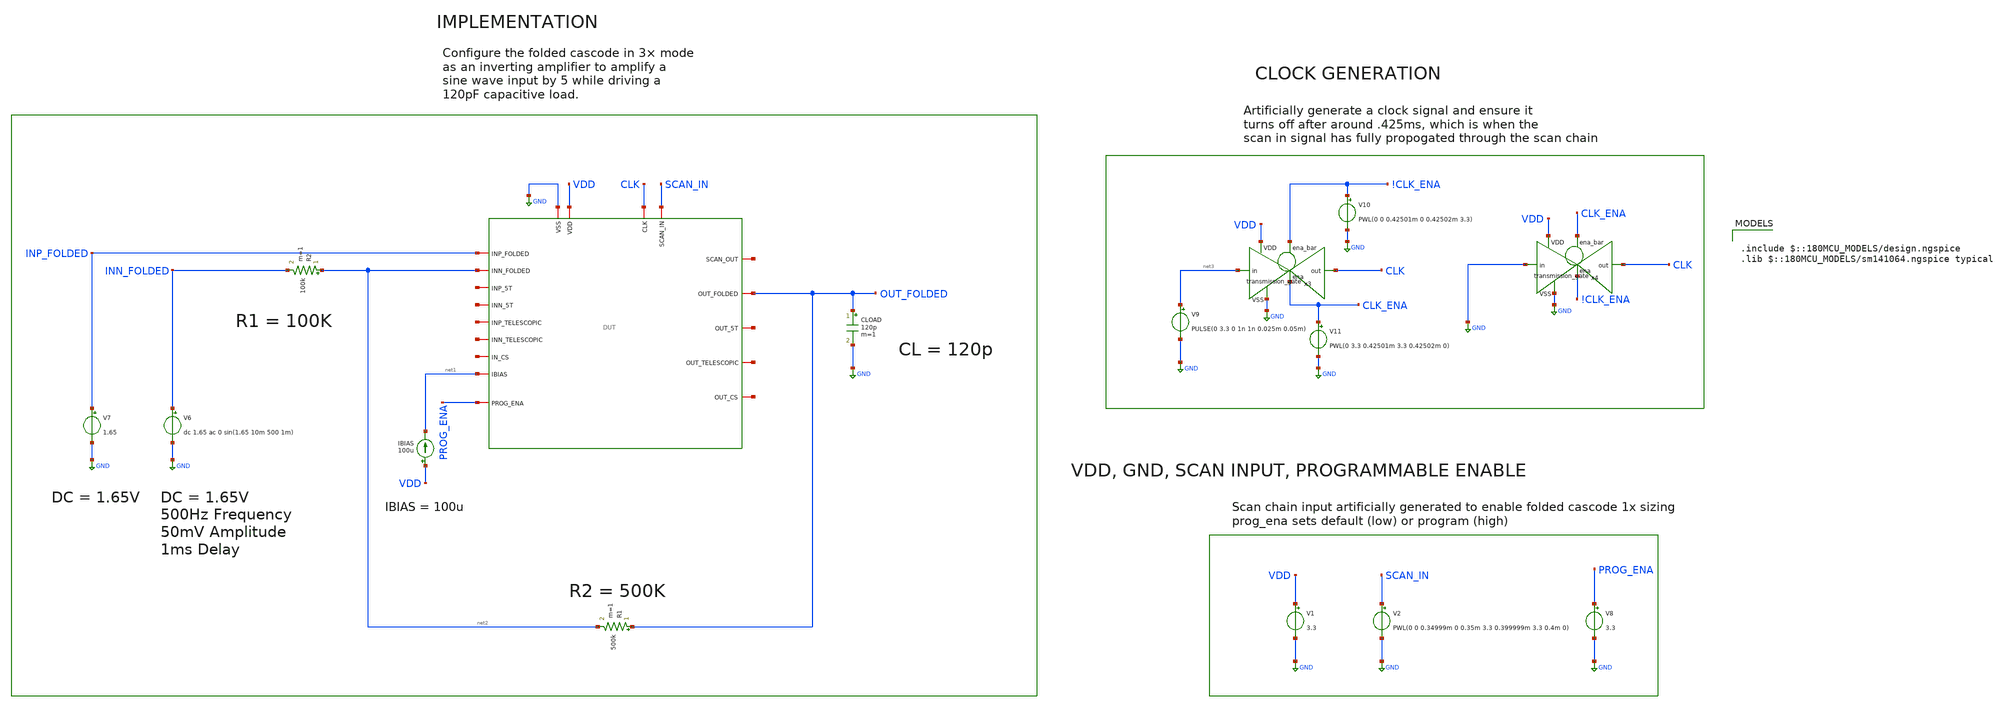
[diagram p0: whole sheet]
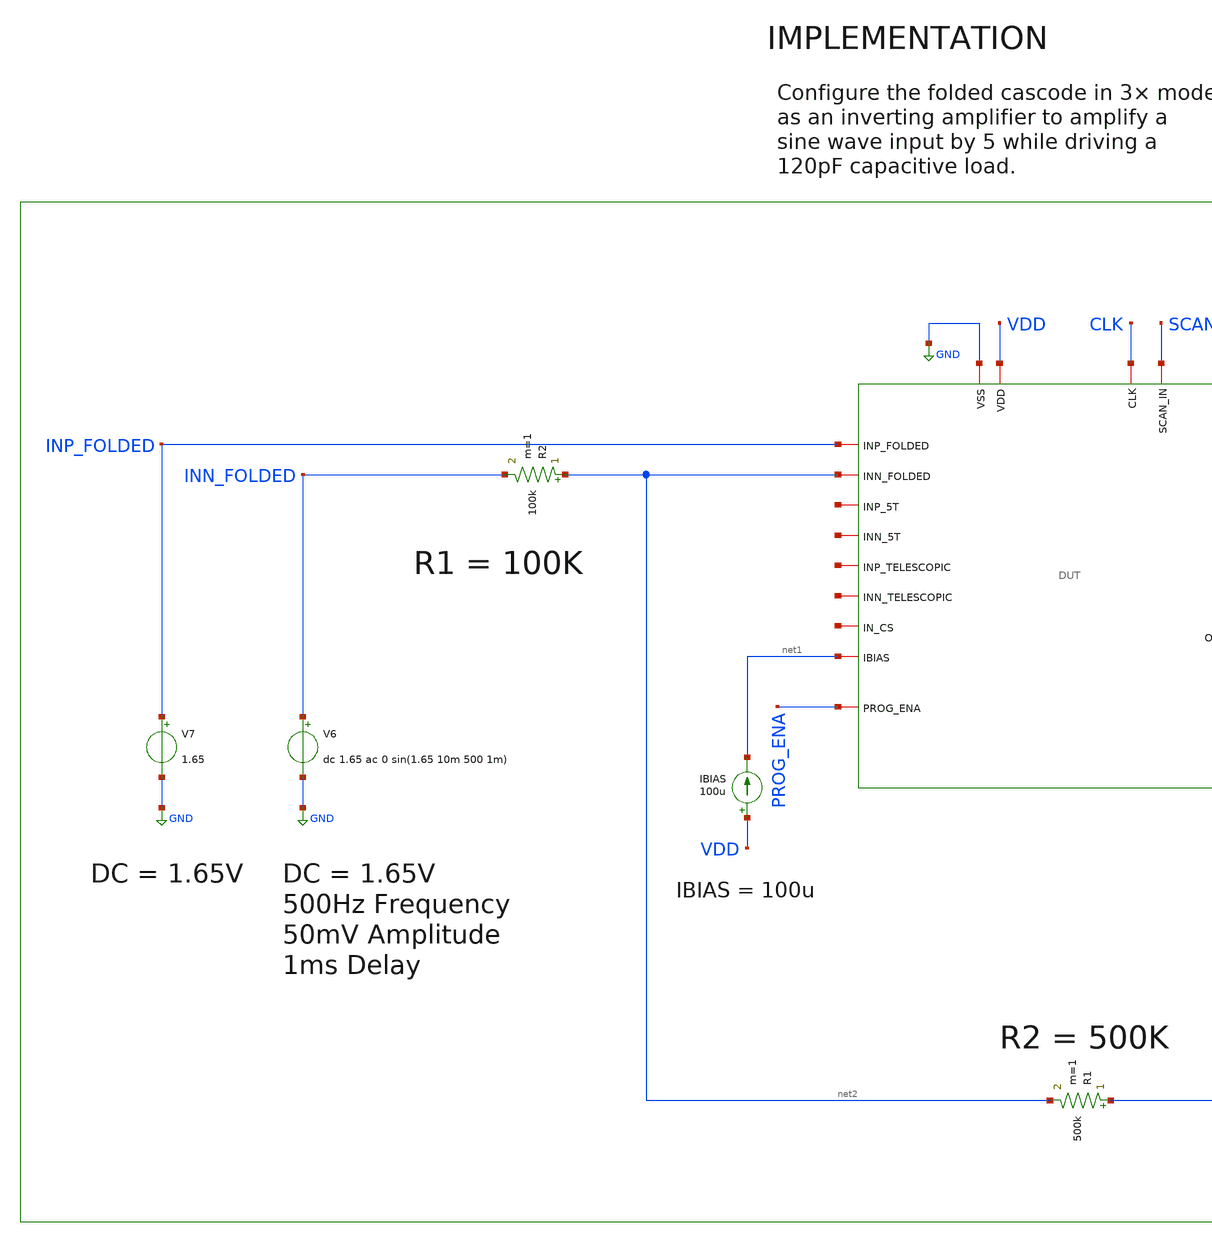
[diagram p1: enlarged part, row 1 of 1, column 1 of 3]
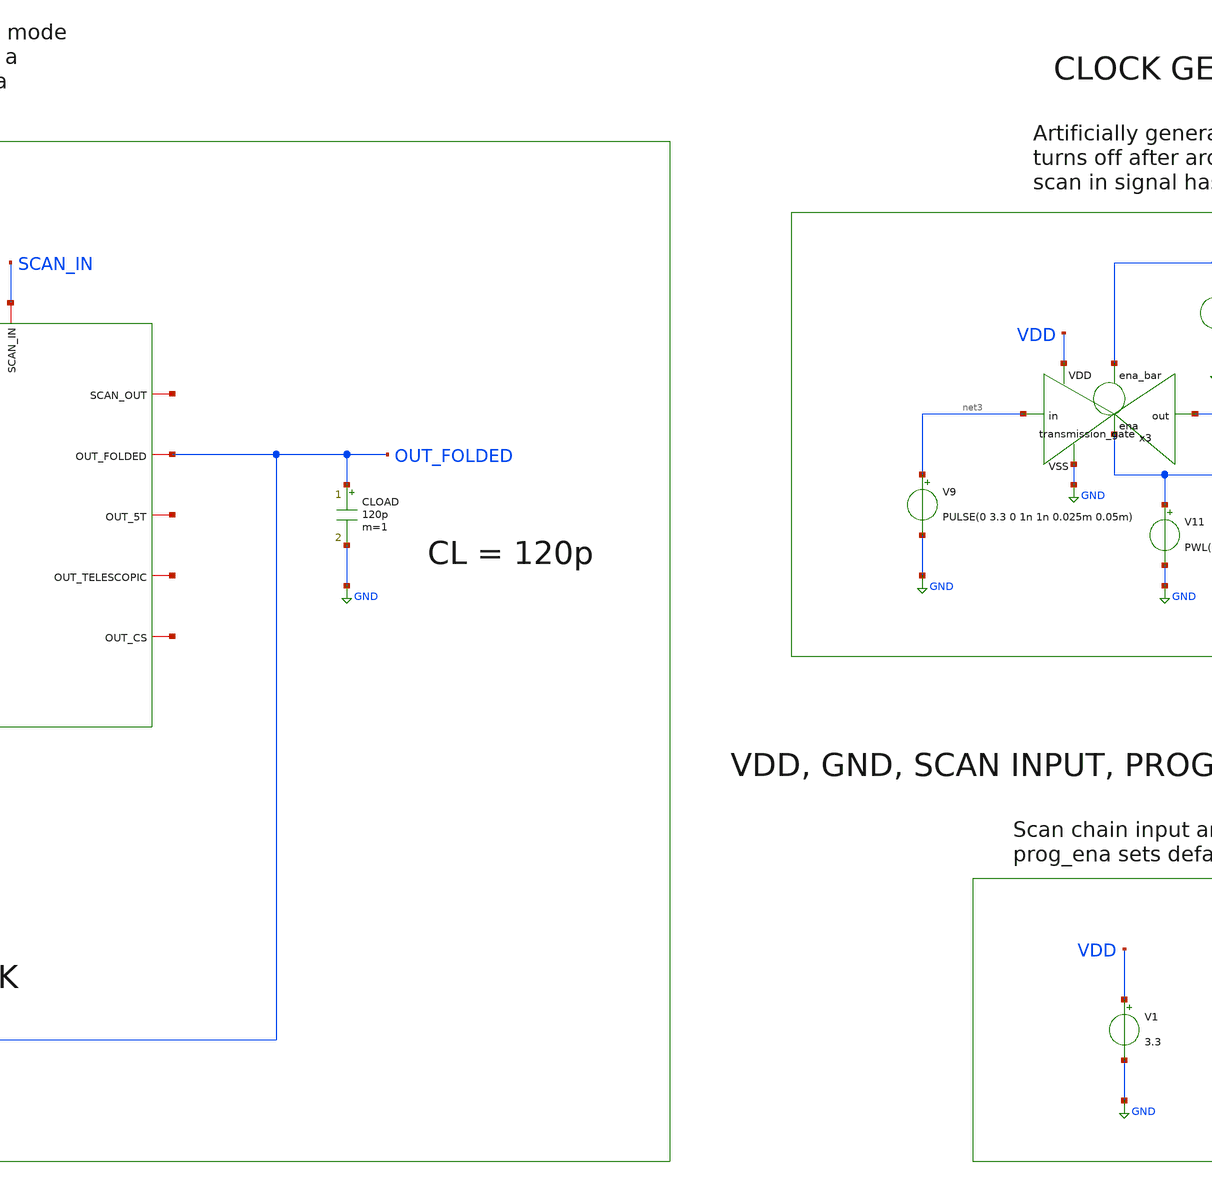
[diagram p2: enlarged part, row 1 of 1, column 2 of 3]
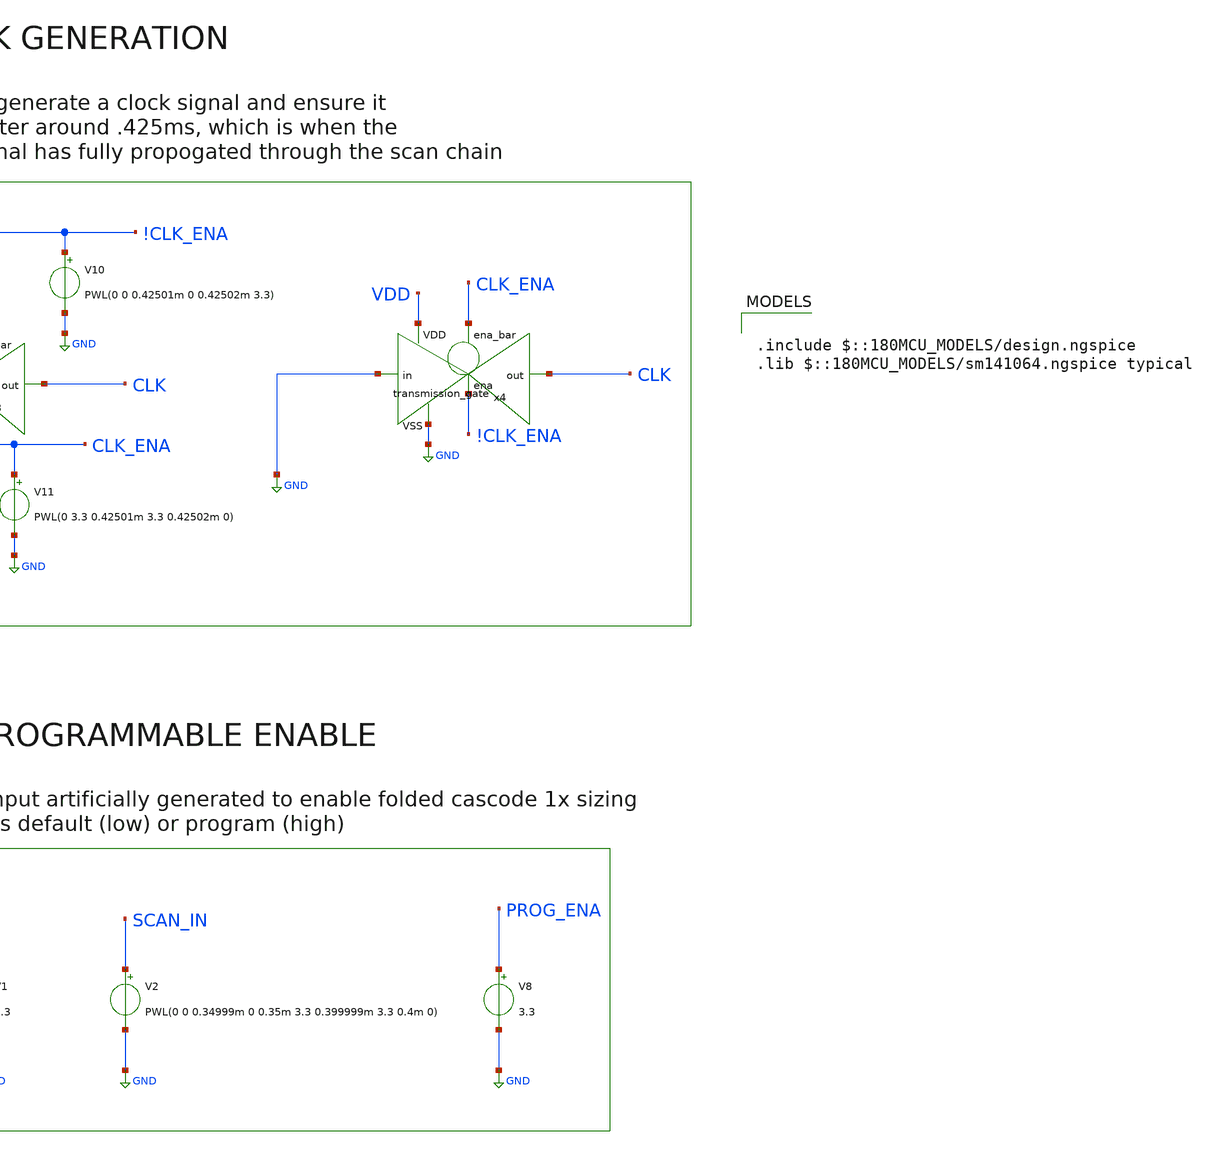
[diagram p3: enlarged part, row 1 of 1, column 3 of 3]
** sch_path: designs/libs/pex/folded/inverting_amplifier/3x.sch
**.subckt 3x
V1 VDD GND 3.3
IBIAS VDD net1 100u
V7 INP_FOLDED GND 1.65
CLOAD OUT_FOLDED GND 120p m=1
R2 net2 INN_FOLDED 100k m=1
V6 INN_FOLDED GND dc 1.65 ac 0 sin(1.65 10m 500 1m)
R1 OUT_FOLDED net2 500k m=1
V8 PROG_ENA GND 3.3
V9 net3 GND PULSE(0 3.3 0 1n 1n 0.025m 0.05m)
x3 !CLK_ENA VDD CLK net3 GND CLK_ENA transmission_gate
V10 !CLK_ENA GND PWL(0 0 0.42501m 0 0.42502m 3.3)
V11 CLK_ENA GND PWL(0 3.3 0.42501m 3.3 0.42502m 0)
x4 CLK_ENA VDD CLK GND GND !CLK_ENA transmission_gate
V2 SCAN_IN GND PWL(0 0 0.34999m 0 0.35m 3.3 0.399999m 3.3 0.4m 0)
x1 CLK net4 SCAN_IN GND VDD OUT_FOLDED INP_FOLDED net5 net1 net2 net6 net7 net8 net9 net10 net11
+ net12 PROG_ENA DUT
**** begin user architecture code

.include $::180MCU_MODELS/design.ngspice
.lib $::180MCU_MODELS/sm141064.ngspice typical



.include /foss/designs/libs/pex/DUT.spice
.control
tran 1u 5m

plot v(out_folded) v(inn_folded)

meas tran vout_pp pp v(out_folded) from=2m to=5m
meas tran vin_pp pp v(inn_folded) from=2m to=5m
let gain = vout_pp / vin_pp
print gain

meas tran vout_dc avg v(out_folded) from=2m to=5m
meas tran vin_dc avg v(inn_folded) from=2m to=5m
let dc_offset = vout_dc - vin_dc
let input_offset = dc_offset / 6
print vout_dc vin_dc dc_offset input_offset

let ideal_gain = 5
let gain_error_pct = (ideal_gain - gain) / ideal_gain * 100
print gain_error_pct

meas tran idd avg i(v1) from=2m to=5m
let power = abs(idd) * 3.3
print idd power
.endc


**** end user architecture code
**.ends

* expanding   symbol:  libs/core_digital/schem/transmission_gate.sym # of pins=6
** sym_path: designs/libs/core_digital/schem/transmission_gate.sym
** sch_path: designs/libs/core_digital/schem/transmission_gate.sch
.subckt transmission_gate ena_bar VDD out in VSS ena
*.ipin in
*.ipin ena_bar
*.ipin ena
*.ipin VSS
*.ipin VDD
*.opin out
XM1 in ena_bar out VDD pfet_03v3 L=0.28u W=0.22u nf=1 ad='int((nf+1)/2) * W/nf * 0.18u' as='int((nf+2)/2) * W/nf * 0.18u'
+ pd='2*int((nf+1)/2) * (W/nf + 0.18u)' ps='2*int((nf+2)/2) * (W/nf + 0.18u)' nrd='0.18u / W' nrs='0.18u / W'
+ sa=0 sb=0 sd=0 m=1
XM2 in ena out VSS nfet_03v3 L=0.28u W=0.22u nf=1 ad='int((nf+1)/2) * W/nf * 0.18u' as='int((nf+2)/2) * W/nf * 0.18u'
+ pd='2*int((nf+1)/2) * (W/nf + 0.18u)' ps='2*int((nf+2)/2) * (W/nf + 0.18u)' nrd='0.18u / W' nrs='0.18u / W'
+ sa=0 sb=0 sd=0 m=1
.ends

.GLOBAL GND
.end
